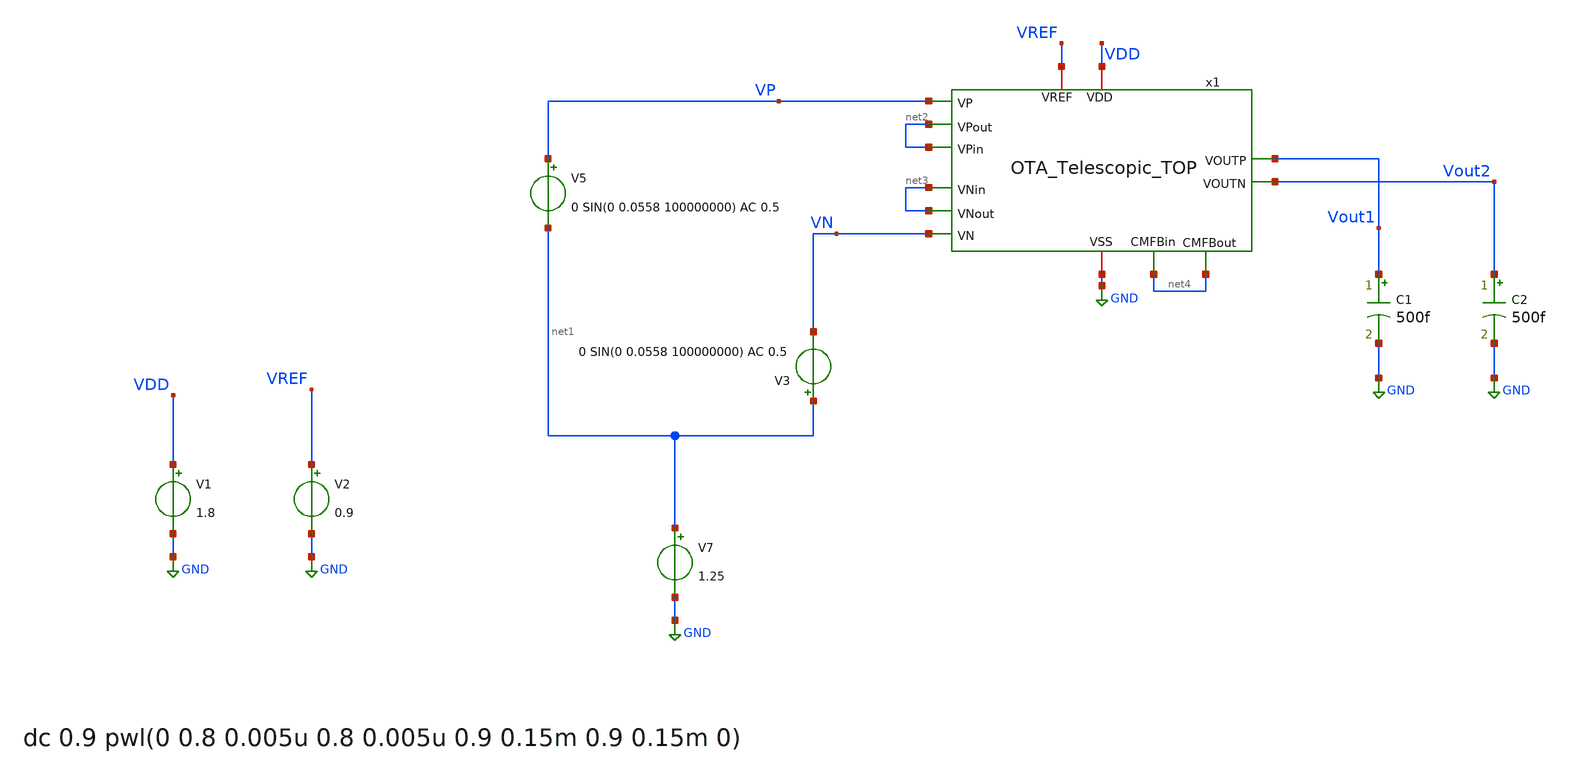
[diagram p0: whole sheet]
** sch_path: OTA_Telescopic/OTA_Telescopic_TOP_TB_CL.sch
**.subckt OTA_Telescopic_TOP_TB_CL
V7 net1 GND 1.25
V5 VP net1 0 SIN(0 0.0558 100000000) AC 0.5
V1 VDD GND 1.8
V2 VREF GND 0.9
C1 Vout1 GND 500f m=1
C2 Vout2 GND 500f m=1
V3 net1 VN 0 SIN(0 0.0558 100000000) AC 0.5
x1 VDD GND net2 VP net2 Vout2 Vout1 net3 net3 VN VREF net4 net4 OTA_Telescopic_TOP
**** begin user architecture code

** opencircuitdesign pdks install
.lib cornerMOSlv.lib mos_tt
.lib cornerRES.lib res_typ
.lib cornerCAP.lib cap_typ
.temp 65



.control
save all
 set color0 = white

* AC simulation
ac dec 1000 1 1T
let Av = db(v(Vout1)-v(Vout2))
meas ac Ao FIND Av WHEN frequency=10
let ABW = Ao-3
meas ac BW WHEN Av=ABW
meas ac UGBW WHEN Av=0
let phase_vec = 180/pi*cph(v(Vout1)-v(Vout2))

* Phase margin (PM)
meas ac phase FIND phase_vec WHEN frequency=UGBW
let PM = phase+180
print PM

* Gain margin (GM)
meas ac freq180 FIND frequency WHEN phase_vec=-180
meas ac gain FIND Av WHEN frequency=freq180
let GM = 0-gain

print GM
plot Av
plot phase_vec

write AC_OL.raw
wrdata AvCL_ Av

*DC simulation

op
let vout_dc = v(Vout1)
print vout_dc
write OTA_Telescopic_TOP_TB_CL.raw

.endc




.op

.save all
*OTA
.save @n.x1.x1.xm1.nsg13_lv_nmos[ids]
.save @n.x1.x1.xm1.nsg13_lv_nmos[gm]
.save @n.x1.x1.xm2.nsg13_lv_nmos[ids]
.save @n.x1.x1.xm2.nsg13_lv_nmos[gm]

.save @n.x1.x1.xm9.nsg13_lv_pmos[ids]
.save @n.x1.x1.xm9.nsg13_lv_pmos[gm]
.save @n.x1.x1.xm10.nsg13_lv_pmos[ids]
.save @n.x1.x1.xm10.nsg13_lv_pmos[gm]

.save @n.x1.x1.xm0.nsg13_lv_nmos[ids]

.save @n.x1.x1.xm1.nsg13_lv_nmos[vsat]


.save @n.x1.x1.xm13.nsg13_lv_nmos[ids]
.save @n.x1.x1.xm14.nsg13_lv_nmos[ids]
.save @n.x1.x1.xm15.nsg13_lv_nmos[ids]
.save @n.x1.x1.xm16.nsg13_lv_nmos[ids]
.save @n.x1.x1.xm17.nsg13_lv_nmos[ids]

.save @n.x1.x1.xm18.nsg13_lv_pmos[ids]
.save @n.x1.x1.xm19.nsg13_lv_pmos[ids]

*CMFB
.save @n.x1.x2.xm0.nsg13_lv_pmos[ids]
.save @n.x1.x2.xm1.nsg13_lv_pmos[ids]
.save @n.x1.x2.xm1.nsg13_lv_pmos[gm]
.save @n.x1.x2.xm2.nsg13_lv_pmos[ids]
.save @n.x1.x2.xm2.nsg13_lv_pmos[gm]
.save @n.x1.x2.xm3.nsg13_lv_pmos[ids]
.save @n.x1.x2.xm3.nsg13_lv_pmos[gm]
.save @n.x1.x2.xm4.nsg13_lv_pmos[ids]
.save @n.x1.x2.xm4.nsg13_lv_pmos[gm]
.save @n.x1.x2.xm5.nsg13_lv_pmos[ids]
.save @n.x1.x2.xm5.nsg13_lv_pmos[gm]
.save @n.x1.x2.xm6.nsg13_lv_pmos[ids]
.save @n.x1.x2.xm6.nsg13_lv_pmos[gm]

.save @n.x1.x2.xm7.nsg13_lv_nmos[ids]
.save @n.x1.x2.xm7.nsg13_lv_nmos[gm]
.save @n.x1.x2.xm8.nsg13_lv_nmos[ids]
.save @n.x1.x2.xm8.nsg13_lv_nmos[gm]



.control

let vsat_M1 = @n.x1.x1.xm1.nsg13_lv_nmos[vsat]
let vsat_M3 = @n.x1.x1.xm3.nsg13_lv_nmos[vsat]
let vsat_M5 = @n.x1.x1.xm5.nsg13_lv_pmos[vsat]
let vsat_M7 = @n.x1.x1.xm7.nsg13_lv_pmos[vsat]
let vsat_M0 = @n.x1.x1.xm0.nsg13_lv_nmos[vsat]

let vsat_M9 = @n.x1.x1.xm9.nsg13_lv_pmos[vsat]
let vsat_M11 = @n.x1.x1.xm11.nsg13_lv_nmos[vsat]

print vsat_M1
print vsat_M3
print vsat_M5
print vsat_M7
print vsat_M0
print vsat_M9
print vsat_M11

let ro_M1 = 1/@n.x1.x1.xm1.nsg13_lv_nmos[gds]
let ro_M3 = 1/@n.x1.x1.xm3.nsg13_lv_nmos[gds]
let ro_M5 = 1/@n.x1.x1.xm5.nsg13_lv_pmos[gds]
let ro_M7 = 1/@n.x1.x1.xm7.nsg13_lv_pmos[gds]
let ro_M0 = 1/@n.x1.x1.xm0.nsg13_lv_nmos[gds]

print ro_M1
print ro_M3
print ro_M5
print ro_M7
print ro_M0

let gm_M1 = @n.x1.x1.xm1.nsg13_lv_nmos[gm]
let gm_M3 = @n.x1.x1.xm3.nsg13_lv_nmos[gm]
let gm_M5 = @n.x1.x1.xm5.nsg13_lv_pmos[gm]
let gm_M7 = @n.x1.x1.xm7.nsg13_lv_pmos[gm]
let gm_M0 = @n.x1.x1.xm0.nsg13_lv_nmos[gm]

print gm_M1
print gm_M3
print gm_M5
print gm_M7
print gm_M0

let gmb_M3 = @n.x1.x1.xm3.nsg13_lv_nmos[gmb]
let gmb_M5 = @n.x1.x1.xm5.nsg13_lv_pmos[gmb]

print gmb_M3
print gmb_M5


*CMFB

let x2_vsat_M0 = @n.x1.x2.xm0.nsg13_lv_pmos[vsat]
let x2_vth_M0 = @n.x1.x2.xm0.nsg13_lv_pmos[vth]

print x2_vsat_M0
print x2_vth_M0

.endc



**** end user architecture code
**.ends
.GLOBAL GND
.end
